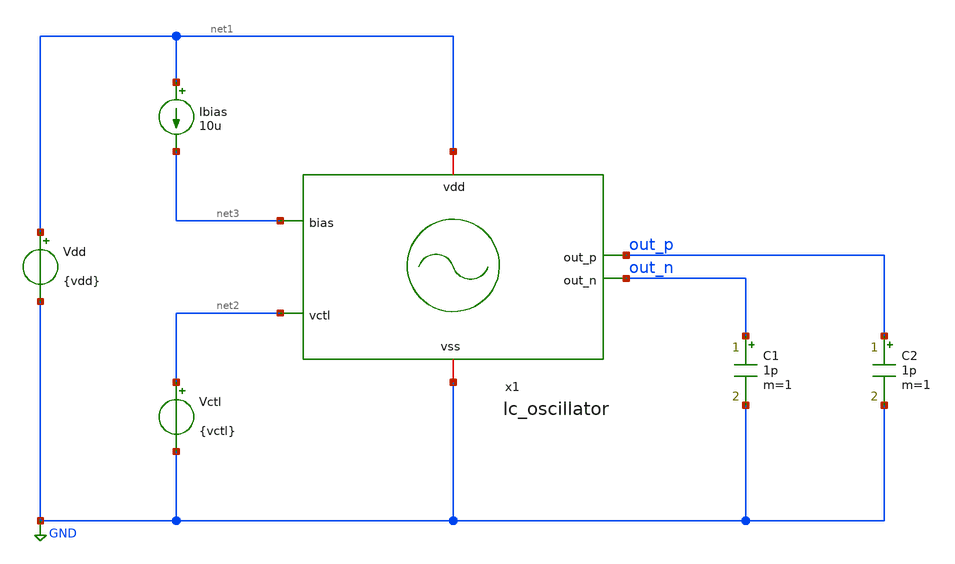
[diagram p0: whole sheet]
** sch_path: design/lc_oscillator/test/lc_oscillator_tb.sch
**.subckt lc_oscillator_tb
x1 net1 out_p net2 out_n net3 GND lc_oscillator
Ibias net1 net3 10u
Vctl net2 GND {vctl}
Vdd net1 GND {vdd}
C1 out_n GND 1p m=1
C2 out_p GND 1p m=1
**** begin user architecture code


.param temp=27

.param vdd=1.8 vctl=0.9

*.op
.tran 1p 300n uic

*.options rshunt=1e11

.save all




.options wnflag=1
.include $::SKYWATER_MODELS/cells/nfet_01v8/sky130_fd_pr__nfet_01v8__tt.corner.spice
.include $::SKYWATER_MODELS/cells/nfet_01v8_lvt/sky130_fd_pr__nfet_01v8_lvt__tt.corner.spice
.include $::SKYWATER_MODELS/cells/pfet_01v8/sky130_fd_pr__pfet_01v8__tt.corner.spice
.include $::SKYWATER_MODELS/cells/nfet_03v3_nvt/sky130_fd_pr__nfet_03v3_nvt__tt.corner.spice
.include $::SKYWATER_MODELS/cells/nfet_05v0_nvt/sky130_fd_pr__nfet_05v0_nvt__tt.corner.spice
.include $::SKYWATER_MODELS/cells/esd_nfet_01v8/sky130_fd_pr__esd_nfet_01v8__tt.corner.spice
.include $::SKYWATER_MODELS/cells/pfet_01v8_lvt/sky130_fd_pr__pfet_01v8_lvt__tt.corner.spice
.include $::SKYWATER_MODELS/cells/pfet_01v8_hvt/sky130_fd_pr__pfet_01v8_hvt__tt.corner.spice
.include $::SKYWATER_MODELS/cells/esd_pfet_g5v0d10v5/sky130_fd_pr__esd_pfet_g5v0d10v5__tt.corner.spice
.include $::SKYWATER_MODELS/cells/pfet_g5v0d10v5/sky130_fd_pr__pfet_g5v0d10v5__tt.corner.spice
.include $::SKYWATER_MODELS/cells/pfet_g5v0d16v0/sky130_fd_pr__pfet_g5v0d16v0__tt.corner.spice
.include $::SKYWATER_MODELS/cells/nfet_g5v0d10v5/sky130_fd_pr__nfet_g5v0d10v5__tt.corner.spice
.include $::SKYWATER_MODELS/cells/nfet_g5v0d16v0/sky130_fd_pr__nfet_g5v0d16v0__tt_discrete.corner.spice
.include $::SKYWATER_MODELS/cells/esd_nfet_g5v0d10v5/sky130_fd_pr__esd_nfet_g5v0d10v5__tt.corner.spice
.include $::SKYWATER_MODELS/models/corners/tt/nonfet.spice
* Mismatch parameters
.include $::SKYWATER_MODELS/cells/nfet_01v8/sky130_fd_pr__nfet_01v8__mismatch.corner.spice
.include $::SKYWATER_MODELS/cells/pfet_01v8/sky130_fd_pr__pfet_01v8__mismatch.corner.spice
.include $::SKYWATER_MODELS/cells/nfet_01v8_lvt/sky130_fd_pr__nfet_01v8_lvt__mismatch.corner.spice
.include $::SKYWATER_MODELS/cells/pfet_01v8_lvt/sky130_fd_pr__pfet_01v8_lvt__mismatch.corner.spice
.include $::SKYWATER_MODELS/cells/pfet_01v8_hvt/sky130_fd_pr__pfet_01v8_hvt__mismatch.corner.spice
.include $::SKYWATER_MODELS/cells/nfet_g5v0d10v5/sky130_fd_pr__nfet_g5v0d10v5__mismatch.corner.spice
.include $::SKYWATER_MODELS/cells/pfet_g5v0d10v5/sky130_fd_pr__pfet_g5v0d10v5__mismatch.corner.spice
.include $::SKYWATER_MODELS/cells/nfet_05v0_nvt/sky130_fd_pr__nfet_05v0_nvt__mismatch.corner.spice
.include $::SKYWATER_MODELS/cells/nfet_03v3_nvt/sky130_fd_pr__nfet_03v3_nvt__mismatch.corner.spice
* Resistor$::SKYWATER_MODELS/Capacitor
.include $::SKYWATER_MODELS/models/r+c/res_typical__cap_typical.spice
.include $::SKYWATER_MODELS/models/r+c/res_typical__cap_typical__lin.spice
* Special cells
.include $::SKYWATER_MODELS/models/corners/tt/specialized_cells.spice
* All models
.include $::SKYWATER_MODELS/models/all.spice
* Corner
.include $::SKYWATER_MODELS/models/corners/tt/rf.spice

 [sky130_models]
**** end user architecture code
**.ends

* expanding   symbol:  lc_oscillator/lc_oscillator.sym # of pins=6
** sym_path: design/lc_oscillator/lc_oscillator.sym
** sch_path: design/lc_oscillator/lc_oscillator.sch
.subckt lc_oscillator vdd out_p vctl out_n bias vss
*.ipin vctl
*.iopin vss
*.ipin bias
*.iopin vdd
*.opin out_p
*.opin out_n
XM2 bias bias vss vss sky130_fd_pr__nfet_01v8_lvt L=0.5 W=5 nf=1 ad='int((nf+1)/2) * W/nf * 0.29' as='int((nf+2)/2) * W/nf * 0.29'
+ pd='2*int((nf+1)/2) * (W/nf + 0.29)' ps='2*int((nf+2)/2) * (W/nf + 0.29)' nrd='0.29 / W' nrs='0.29 / W'
+ sa=0 sb=0 sd=0 mult=1 m=1
XM1 net4 bias vss vss sky130_fd_pr__nfet_01v8_lvt L=0.5 W=5 nf=1 ad='int((nf+1)/2) * W/nf * 0.29' as='int((nf+2)/2) * W/nf * 0.29'
+ pd='2*int((nf+1)/2) * (W/nf + 0.29)' ps='2*int((nf+2)/2) * (W/nf + 0.29)' nrd='0.29 / W' nrs='0.29 / W'
+ sa=0 sb=0 sd=0 mult=64 m=64
XM3 net3 bias vss vss sky130_fd_pr__nfet_01v8_lvt L=0.5 W=5 nf=1 ad='int((nf+1)/2) * W/nf * 0.29' as='int((nf+2)/2) * W/nf * 0.29'
+ pd='2*int((nf+1)/2) * (W/nf + 0.29)' ps='2*int((nf+2)/2) * (W/nf + 0.29)' nrd='0.29 / W' nrs='0.29 / W'
+ sa=0 sb=0 sd=0 mult=64 m=64
XC1 osc_p net2 sky130_fd_pr__cap_mim_m3_1 W=6 L=6 MF=4 m=4
XC2 osc_n net1 sky130_fd_pr__cap_mim_m3_1 W=6 L=6 MF=4 m=4
XC3 net2 net5 sky130_fd_pr__cap_mim_m3_1 W=6 L=6 MF=1 m=1
XC4 net1 net5 sky130_fd_pr__cap_mim_m3_1 W=6 L=6 MF=1 m=1
XM4 osc_p vdd net2 vss sky130_fd_pr__nfet_01v8_lvt L=0.15 W=20 nf=1 ad='int((nf+1)/2) * W/nf * 0.29'
+ as='int((nf+2)/2) * W/nf * 0.29' pd='2*int((nf+1)/2) * (W/nf + 0.29)' ps='2*int((nf+2)/2) * (W/nf + 0.29)'
+ nrd='0.29 / W' nrs='0.29 / W' sa=0 sb=0 sd=0 mult=1 m=1
XM5 osc_n vdd net1 vss sky130_fd_pr__nfet_01v8_lvt L=0.15 W=20 nf=1 ad='int((nf+1)/2) * W/nf * 0.29'
+ as='int((nf+2)/2) * W/nf * 0.29' pd='2*int((nf+1)/2) * (W/nf + 0.29)' ps='2*int((nf+2)/2) * (W/nf + 0.29)'
+ nrd='0.29 / W' nrs='0.29 / W' sa=0 sb=0 sd=0 mult=1 m=1
L1 vdd osc_p vss lc_oscillator_inductor
L2 vdd osc_n vss lc_oscillator_inductor
XM6 net2 net1 net3 vss sky130_fd_pr__nfet_01v8_lvt L=0.15 W=20 nf=1 ad='int((nf+1)/2) * W/nf * 0.29'
+ as='int((nf+2)/2) * W/nf * 0.29' pd='2*int((nf+1)/2) * (W/nf + 0.29)' ps='2*int((nf+2)/2) * (W/nf + 0.29)'
+ nrd='0.29 / W' nrs='0.29 / W' sa=0 sb=0 sd=0 mult=1 m=1
XM7 net1 net2 net4 vss sky130_fd_pr__nfet_01v8_lvt L=0.15 W=20 nf=1 ad='int((nf+1)/2) * W/nf * 0.29'
+ as='int((nf+2)/2) * W/nf * 0.29' pd='2*int((nf+1)/2) * (W/nf + 0.29)' ps='2*int((nf+2)/2) * (W/nf + 0.29)'
+ nrd='0.29 / W' nrs='0.29 / W' sa=0 sb=0 sd=0 mult=1 m=1
XC5 vdd vss sky130_fd_pr__cap_mim_m3_1 W=10 L=10 MF=4 m=4
x1 vctl osc_p lc_oscillator_varactor
x2 vctl osc_n lc_oscillator_varactor
XM8 out_n out_p vss vss sky130_fd_pr__nfet_01v8_lvt L=0.15 W=20 nf=1 ad='int((nf+1)/2) * W/nf * 0.29'
+ as='int((nf+2)/2) * W/nf * 0.29' pd='2*int((nf+1)/2) * (W/nf + 0.29)' ps='2*int((nf+2)/2) * (W/nf + 0.29)'
+ nrd='0.29 / W' nrs='0.29 / W' sa=0 sb=0 sd=0 mult=1 m=1
XM9 out_p out_n vss vss sky130_fd_pr__nfet_01v8_lvt L=0.15 W=20 nf=1 ad='int((nf+1)/2) * W/nf * 0.29'
+ as='int((nf+2)/2) * W/nf * 0.29' pd='2*int((nf+1)/2) * (W/nf + 0.29)' ps='2*int((nf+2)/2) * (W/nf + 0.29)'
+ nrd='0.29 / W' nrs='0.29 / W' sa=0 sb=0 sd=0 mult=1 m=1
XM10 out_n net6 vss vss sky130_fd_pr__nfet_01v8_lvt L=0.15 W=20 nf=1 ad='int((nf+1)/2) * W/nf * 0.29'
+ as='int((nf+2)/2) * W/nf * 0.29' pd='2*int((nf+1)/2) * (W/nf + 0.29)' ps='2*int((nf+2)/2) * (W/nf + 0.29)'
+ nrd='0.29 / W' nrs='0.29 / W' sa=0 sb=0 sd=0 mult=1 m=1
XM11 out_p net7 vss vss sky130_fd_pr__nfet_01v8_lvt L=0.15 W=20 nf=1 ad='int((nf+1)/2) * W/nf * 0.29'
+ as='int((nf+2)/2) * W/nf * 0.29' pd='2*int((nf+1)/2) * (W/nf + 0.29)' ps='2*int((nf+2)/2) * (W/nf + 0.29)'
+ nrd='0.29 / W' nrs='0.29 / W' sa=0 sb=0 sd=0 mult=1 m=1
XR1 out_n net6 vss sky130_fd_pr__res_xhigh_po_0p35 L=40 mult=1 m=1
XR2 out_p net7 vss sky130_fd_pr__res_xhigh_po_0p35 L=40 mult=1 m=1
XC6 osc_n net6 sky130_fd_pr__cap_mim_m3_1 W=4 L=4 MF=1 m=1
XC7 osc_p net7 sky130_fd_pr__cap_mim_m3_1 W=4 L=4 MF=1 m=1
XM16 out_n net6 vdd vdd sky130_fd_pr__pfet_01v8_hvt L=0.15 W=3 nf=1 ad='int((nf+1)/2) * W/nf * 0.29'
+ as='int((nf+2)/2) * W/nf * 0.29' pd='2*int((nf+1)/2) * (W/nf + 0.29)' ps='2*int((nf+2)/2) * (W/nf + 0.29)'
+ nrd='0.29 / W' nrs='0.29 / W' sa=0 sb=0 sd=0 mult=1 m=1
XM14 out_p net7 vdd vdd sky130_fd_pr__pfet_01v8_hvt L=0.15 W=3 nf=1 ad='int((nf+1)/2) * W/nf * 0.29'
+ as='int((nf+2)/2) * W/nf * 0.29' pd='2*int((nf+1)/2) * (W/nf + 0.29)' ps='2*int((nf+2)/2) * (W/nf + 0.29)'
+ nrd='0.29 / W' nrs='0.29 / W' sa=0 sb=0 sd=0 mult=1 m=1
XM12 out_p out_n vdd vdd sky130_fd_pr__pfet_01v8_hvt L=0.15 W=1 nf=1 ad='int((nf+1)/2) * W/nf * 0.29'
+ as='int((nf+2)/2) * W/nf * 0.29' pd='2*int((nf+1)/2) * (W/nf + 0.29)' ps='2*int((nf+2)/2) * (W/nf + 0.29)'
+ nrd='0.29 / W' nrs='0.29 / W' sa=0 sb=0 sd=0 mult=1 m=1
XM13 out_n out_p vdd vdd sky130_fd_pr__pfet_01v8_hvt L=0.15 W=1 nf=1 ad='int((nf+1)/2) * W/nf * 0.29'
+ as='int((nf+2)/2) * W/nf * 0.29' pd='2*int((nf+1)/2) * (W/nf + 0.29)' ps='2*int((nf+2)/2) * (W/nf + 0.29)'
+ nrd='0.29 / W' nrs='0.29 / W' sa=0 sb=0 sd=0 mult=1 m=1
.ends


* expanding   symbol:  lc_oscillator_inductor/lc_oscillator_inductor.sym # of pins=3
** sym_path: design/lc_oscillator_inductor/lc_oscillator_inductor.sym
** sch_path: design/lc_oscillator_inductor/lc_oscillator_inductor.sch
.subckt lc_oscillator_inductor p1 p2 sub
*.iopin p2
*.iopin p1
*.iopin sub
L1 net1 p1 1.028n m=1
C1 p1 net2 62.02f m=1
R1 net2 sub 16.03 m=1
C2 p1 p2 0.1f m=1
C3 p2 net3 62.31f m=1
R2 net3 sub 15.88 m=1
R3 p2 net1 3.6825 m=1
.ends


* expanding   symbol:  lc_oscillator_varactor/lc_oscillator_varactor.sym # of pins=2
** sym_path: design/lc_oscillator_varactor/lc_oscillator_varactor.sym
** sch_path: design/lc_oscillator_varactor/lc_oscillator_varactor.sch
.subckt lc_oscillator_varactor p m
*.iopin p
*.iopin m
XMvaractor p m p p sky130_fd_pr__nfet_01v8 L=4 W=4 nf=3 ad='int((nf+1)/2) * W/nf * 0.29' as='int((nf+2)/2) * W/nf * 0.29'
+ pd='2*int((nf+1)/2) * (W/nf + 0.29)' ps='2*int((nf+2)/2) * (W/nf + 0.29)' nrd='0.29 / W' nrs='0.29 / W'
+ sa=0 sb=0 sd=0 mult=1 m=1
.ends

.GLOBAL GND
.end
